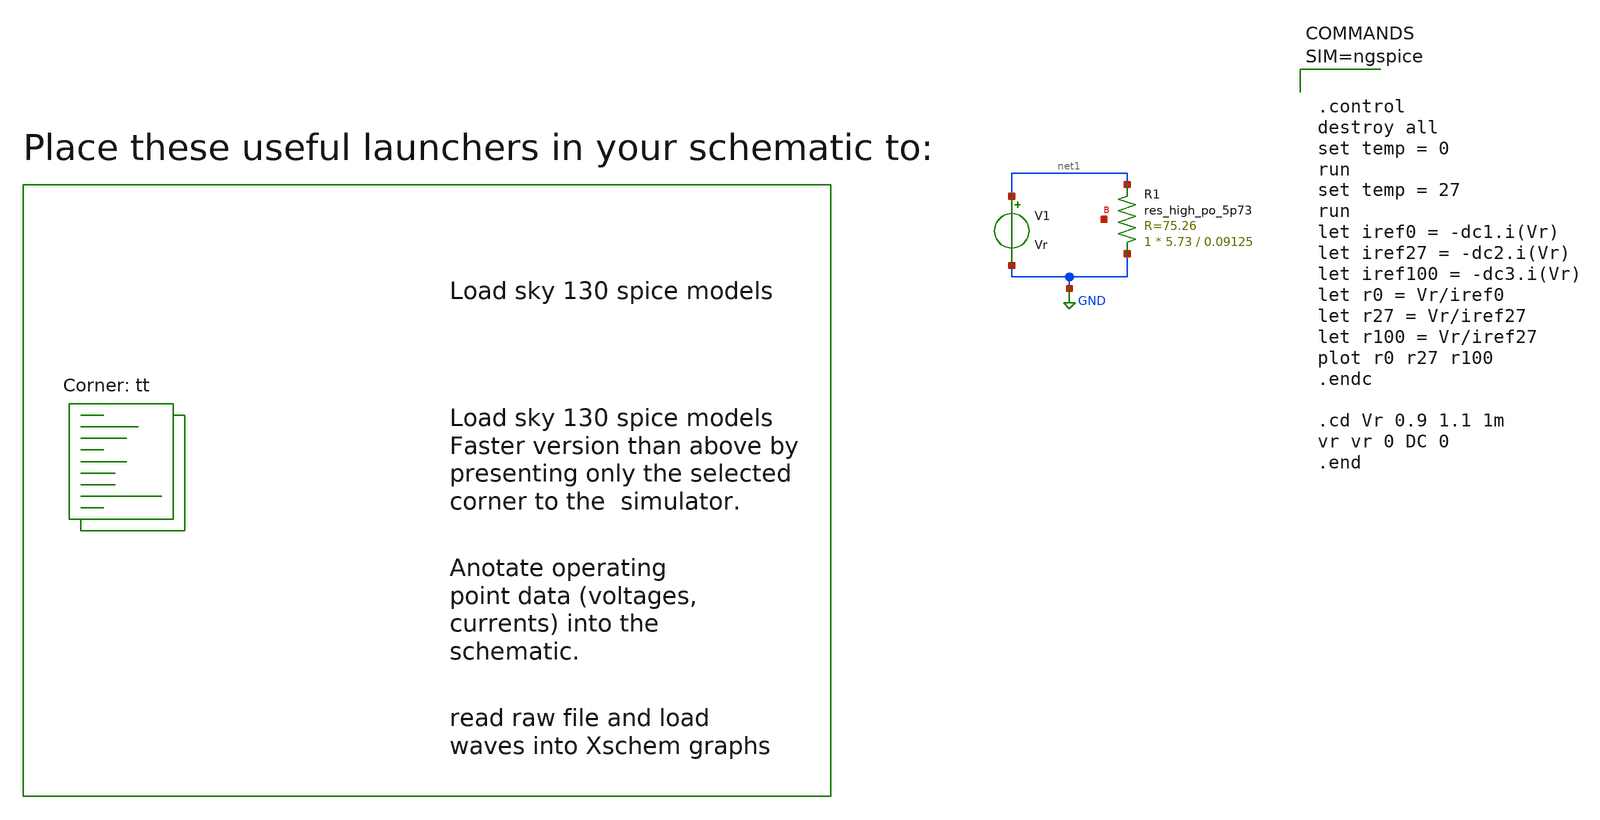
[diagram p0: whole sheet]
** sch_path: termination_resistor/resistor_modelling.sch
**.subckt resistor_modelling
XR1 GND net1 net2 sky130_fd_pr__res_high_po_5p73 L=0.09125 mult=1 m=1
V1 net1 GND Vr
.save i(v1)
**** begin user architecture code



.control
destroy all
set temp = 0
run
set temp = 27
run
let iref0 = -dc1.i(Vr)
let iref27 = -dc2.i(Vr)
let iref100 = -dc3.i(Vr)
let r0 = Vr/iref0
let r27 = Vr/iref27
let r100 = Vr/iref27
plot r0 r27 r100
.endc

.cd Vr 0.9 1.1 1m
vr vr 0 DC 0
.end




** opencircuitdesign pdks install
.lib $::SKYWATER_MODELS/sky130.lib.spice tt

.lib $::SKYWATER_MODELS/sky130.lib.spice tt
**** end user architecture code
**.ends
.GLOBAL GND
.end
